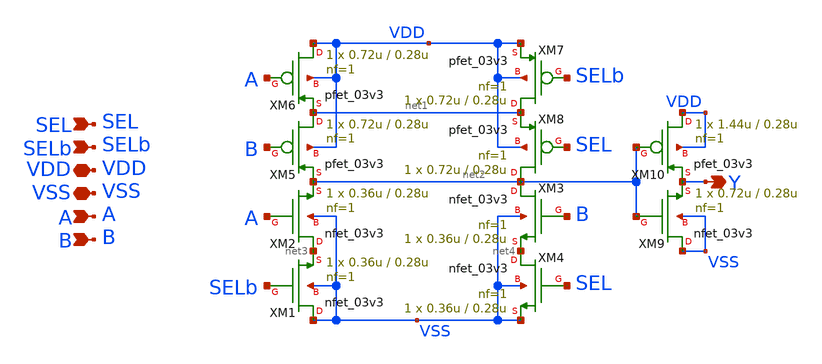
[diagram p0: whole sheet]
** sch_path: CAD4/2x1_mux_cmos.sch
**.subckt 2x1_mux_cmos A B SEL Y VDD VSS SELb
*.ipin A
*.ipin B
*.ipin SEL
*.opin Y
*.iopin VDD
*.iopin VSS
*.ipin SELb
XM1 VSS SELb net3 VSS nfet_03v3 L=0.28u W=0.36u nf=1 ad='int((nf+1)/2) * W/nf * 0.18u' as='int((nf+2)/2) * W/nf * 0.18u'
+ pd='2*int((nf+1)/2) * (W/nf + 0.18u)' ps='2*int((nf+2)/2) * (W/nf + 0.18u)' nrd='0.18u / W' nrs='0.18u / W'
+ sa=0 sb=0 sd=0 m=1
XM2 net3 A net2 VSS nfet_03v3 L=0.28u W=0.36u nf=1 ad='int((nf+1)/2) * W/nf * 0.18u' as='int((nf+2)/2) * W/nf * 0.18u'
+ pd='2*int((nf+1)/2) * (W/nf + 0.18u)' ps='2*int((nf+2)/2) * (W/nf + 0.18u)' nrd='0.18u / W' nrs='0.18u / W'
+ sa=0 sb=0 sd=0 m=1
XM3 net2 B net4 VSS nfet_03v3 L=0.28u W=0.36u nf=1 ad='int((nf+1)/2) * W/nf * 0.18u' as='int((nf+2)/2) * W/nf * 0.18u'
+ pd='2*int((nf+1)/2) * (W/nf + 0.18u)' ps='2*int((nf+2)/2) * (W/nf + 0.18u)' nrd='0.18u / W' nrs='0.18u / W'
+ sa=0 sb=0 sd=0 m=1
XM4 net4 SEL VSS VSS nfet_03v3 L=0.28u W=0.36u nf=1 ad='int((nf+1)/2) * W/nf * 0.18u' as='int((nf+2)/2) * W/nf * 0.18u'
+ pd='2*int((nf+1)/2) * (W/nf + 0.18u)' ps='2*int((nf+2)/2) * (W/nf + 0.18u)' nrd='0.18u / W' nrs='0.18u / W'
+ sa=0 sb=0 sd=0 m=1
XM5 net1 B net2 VDD pfet_03v3 L=0.28u W=0.72u nf=1 ad='int((nf+1)/2) * W/nf * 0.18u' as='int((nf+2)/2) * W/nf * 0.18u'
+ pd='2*int((nf+1)/2) * (W/nf + 0.18u)' ps='2*int((nf+2)/2) * (W/nf + 0.18u)' nrd='0.18u / W' nrs='0.18u / W'
+ sa=0 sb=0 sd=0 m=1
XM6 VDD A net1 VDD pfet_03v3 L=0.28u W=0.72u nf=1 ad='int((nf+1)/2) * W/nf * 0.18u' as='int((nf+2)/2) * W/nf * 0.18u'
+ pd='2*int((nf+1)/2) * (W/nf + 0.18u)' ps='2*int((nf+2)/2) * (W/nf + 0.18u)' nrd='0.18u / W' nrs='0.18u / W'
+ sa=0 sb=0 sd=0 m=1
XM7 net1 SELb VDD VDD pfet_03v3 L=0.28u W=0.72u nf=1 ad='int((nf+1)/2) * W/nf * 0.18u' as='int((nf+2)/2) * W/nf * 0.18u'
+ pd='2*int((nf+1)/2) * (W/nf + 0.18u)' ps='2*int((nf+2)/2) * (W/nf + 0.18u)' nrd='0.18u / W' nrs='0.18u / W'
+ sa=0 sb=0 sd=0 m=1
XM8 net2 SEL net1 VDD pfet_03v3 L=0.28u W=0.72u nf=1 ad='int((nf+1)/2) * W/nf * 0.18u' as='int((nf+2)/2) * W/nf * 0.18u'
+ pd='2*int((nf+1)/2) * (W/nf + 0.18u)' ps='2*int((nf+2)/2) * (W/nf + 0.18u)' nrd='0.18u / W' nrs='0.18u / W'
+ sa=0 sb=0 sd=0 m=1
XM9 VSS net2 Y VSS nfet_03v3 L=0.28u W=0.72u nf=1 ad='int((nf+1)/2) * W/nf * 0.18u' as='int((nf+2)/2) * W/nf * 0.18u'
+ pd='2*int((nf+1)/2) * (W/nf + 0.18u)' ps='2*int((nf+2)/2) * (W/nf + 0.18u)' nrd='0.18u / W' nrs='0.18u / W'
+ sa=0 sb=0 sd=0 m=1
XM10 VDD net2 Y VDD pfet_03v3 L=0.28u W=1.44u nf=1 ad='int((nf+1)/2) * W/nf * 0.18u' as='int((nf+2)/2) * W/nf * 0.18u'
+ pd='2*int((nf+1)/2) * (W/nf + 0.18u)' ps='2*int((nf+2)/2) * (W/nf + 0.18u)' nrd='0.18u / W' nrs='0.18u / W'
+ sa=0 sb=0 sd=0 m=1
**.ends
.end
